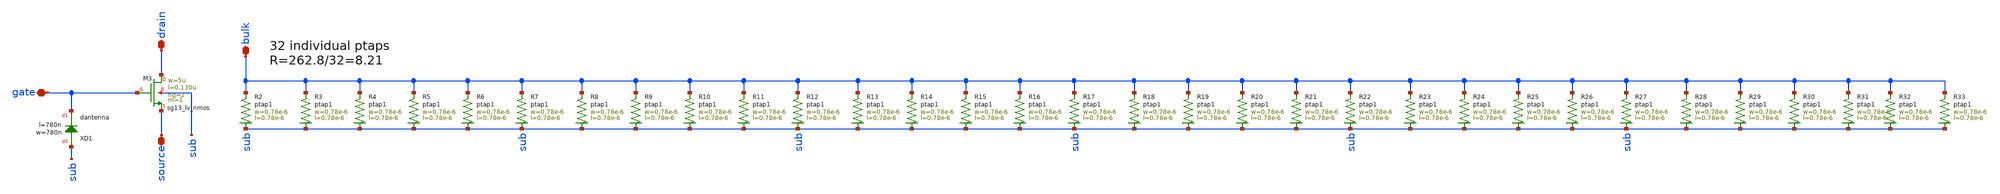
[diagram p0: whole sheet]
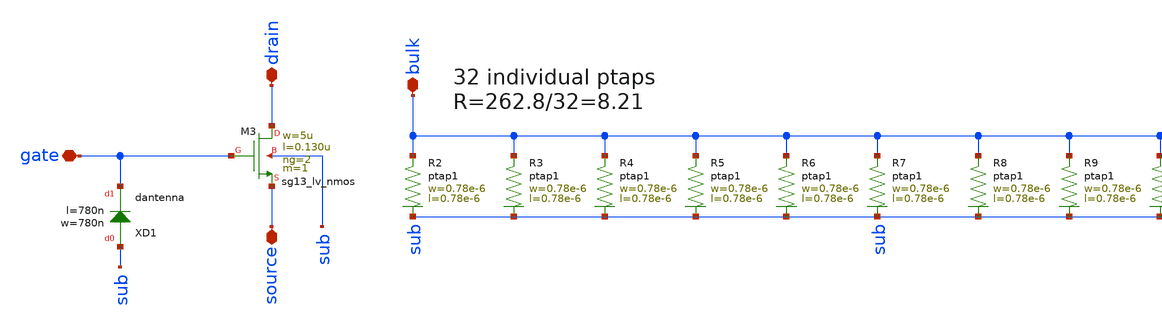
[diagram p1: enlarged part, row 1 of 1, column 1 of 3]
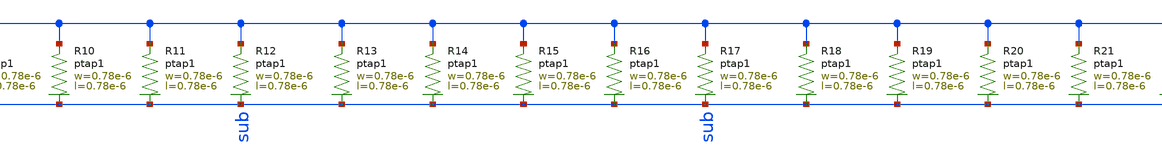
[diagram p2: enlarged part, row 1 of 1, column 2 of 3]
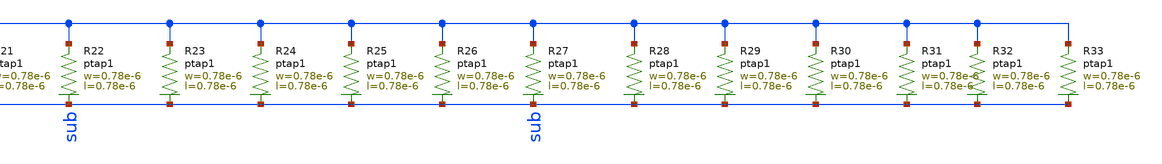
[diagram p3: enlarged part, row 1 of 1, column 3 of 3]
** sch_path: ts_pr_May2024/design_data/xschem/nmos2.sch
**.subckt nmos2 drain source gate bulk
*.iopin drain
*.iopin source
*.iopin gate
*.iopin bulk
XM3 drain gate source sub sg13_lv_nmos w=5u l=0.130u ng=2 m=1 mm_ok=1
XXD1 sub gate dantenna l=780n w=780n
XR2 bulk sub ptap1 R=262.8 w=0.78e-6 l=0.78e-6
XR3 bulk sub ptap1 R=262.8 w=0.78e-6 l=0.78e-6
XR4 bulk sub ptap1 R=262.8 w=0.78e-6 l=0.78e-6
XR5 bulk sub ptap1 R=262.8 w=0.78e-6 l=0.78e-6
XR6 bulk sub ptap1 R=262.8 w=0.78e-6 l=0.78e-6
XR7 bulk sub ptap1 R=262.8 w=0.78e-6 l=0.78e-6
XR8 bulk sub ptap1 R=262.8 w=0.78e-6 l=0.78e-6
XR9 bulk sub ptap1 R=262.8 w=0.78e-6 l=0.78e-6
XR10 bulk sub ptap1 R=262.8 w=0.78e-6 l=0.78e-6
XR11 bulk sub ptap1 R=262.8 w=0.78e-6 l=0.78e-6
XR12 bulk sub ptap1 R=262.8 w=0.78e-6 l=0.78e-6
XR13 bulk sub ptap1 R=262.8 w=0.78e-6 l=0.78e-6
XR14 bulk sub ptap1 R=262.8 w=0.78e-6 l=0.78e-6
XR15 bulk sub ptap1 R=262.8 w=0.78e-6 l=0.78e-6
XR16 bulk sub ptap1 R=262.8 w=0.78e-6 l=0.78e-6
XR17 bulk sub ptap1 R=262.8 w=0.78e-6 l=0.78e-6
XR18 bulk sub ptap1 R=262.8 w=0.78e-6 l=0.78e-6
XR19 bulk sub ptap1 R=262.8 w=0.78e-6 l=0.78e-6
XR20 bulk sub ptap1 R=262.8 w=0.78e-6 l=0.78e-6
XR21 bulk sub ptap1 R=262.8 w=0.78e-6 l=0.78e-6
XR22 bulk sub ptap1 R=262.8 w=0.78e-6 l=0.78e-6
XR23 bulk sub ptap1 R=262.8 w=0.78e-6 l=0.78e-6
XR24 bulk sub ptap1 R=262.8 w=0.78e-6 l=0.78e-6
XR25 bulk sub ptap1 R=262.8 w=0.78e-6 l=0.78e-6
XR26 bulk sub ptap1 R=262.8 w=0.78e-6 l=0.78e-6
XR27 bulk sub ptap1 R=262.8 w=0.78e-6 l=0.78e-6
XR28 bulk sub ptap1 R=262.8 w=0.78e-6 l=0.78e-6
XR29 bulk sub ptap1 R=262.8 w=0.78e-6 l=0.78e-6
XR30 bulk sub ptap1 R=262.8 w=0.78e-6 l=0.78e-6
XR31 bulk sub ptap1 R=262.8 w=0.78e-6 l=0.78e-6
XR32 bulk sub ptap1 R=262.8 w=0.78e-6 l=0.78e-6
XR33 bulk sub ptap1 R=262.8 w=0.78e-6 l=0.78e-6
**.ends
.end
